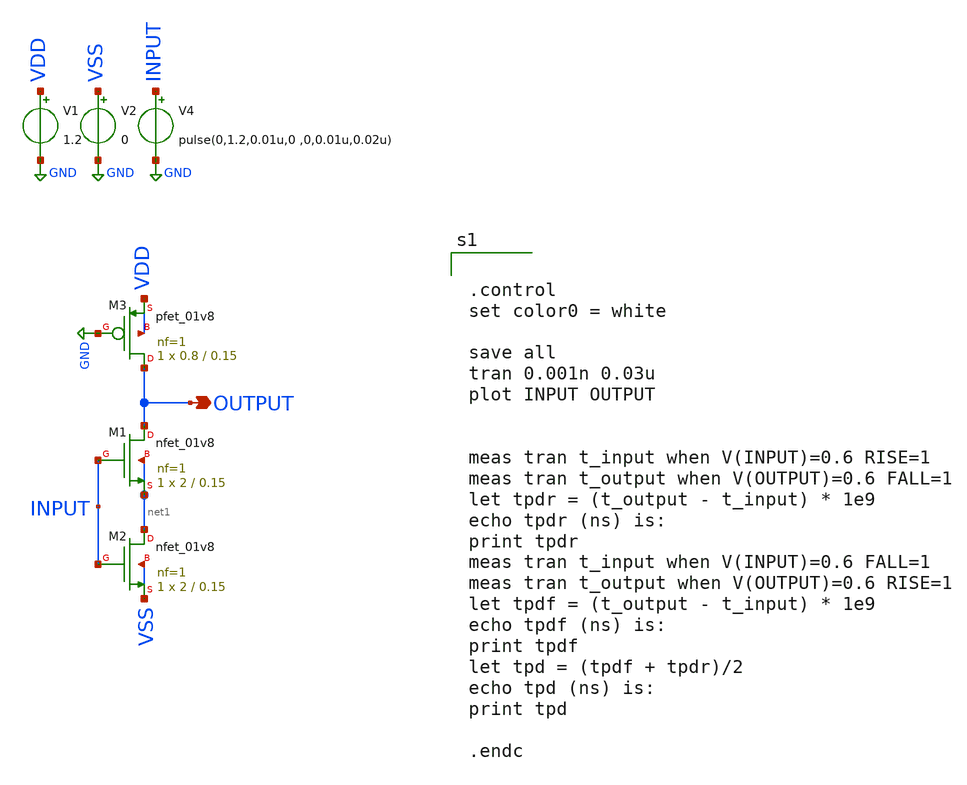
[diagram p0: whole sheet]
** sch_path: design/xschem/pseudo_nand2_tb.sch
**.subckt pseudo_nand2_tb OUTPUT
*.opin OUTPUT
V1 VDD GND 1.2
V2 VSS GND 0
V4 INPUT GND pulse(0,1.2,0.01u,0 ,0,0.01u,0.02u)
XM1 OUTPUT INPUT net1 net1 sky130_fd_pr__nfet_01v8 L=0.15 W=2 nf=1 ad='int((nf+1)/2) * W/nf * 0.29' as='int((nf+2)/2) * W/nf * 0.29'
+ pd='2*int((nf+1)/2) * (W/nf + 0.29)' ps='2*int((nf+2)/2) * (W/nf + 0.29)' nrd='0.29 / W' nrs='0.29 / W'
+ sa=0 sb=0 sd=0 mult=1 m=1
XM2 net1 INPUT VSS VSS sky130_fd_pr__nfet_01v8 L=0.15 W=2 nf=1 ad='int((nf+1)/2) * W/nf * 0.29' as='int((nf+2)/2) * W/nf * 0.29'
+ pd='2*int((nf+1)/2) * (W/nf + 0.29)' ps='2*int((nf+2)/2) * (W/nf + 0.29)' nrd='0.29 / W' nrs='0.29 / W'
+ sa=0 sb=0 sd=0 mult=1 m=1
XM3 OUTPUT GND VDD VDD sky130_fd_pr__pfet_01v8 L=0.15 W=0.8 nf=1 ad='int((nf+1)/2) * W/nf * 0.29' as='int((nf+2)/2) * W/nf * 0.29'
+ pd='2*int((nf+1)/2) * (W/nf + 0.29)' ps='2*int((nf+2)/2) * (W/nf + 0.29)' nrd='0.29 / W' nrs='0.29 / W'
+ sa=0 sb=0 sd=0 mult=1 m=1
**** begin user architecture code

** opencircuitdesign pdks install
.lib $::SKYWATER_MODELS/sky130.lib.spice tt_mm




.control
set color0 = white

save all
tran 0.001n 0.03u
plot INPUT OUTPUT


meas tran t_input when V(INPUT)=0.6 RISE=1
meas tran t_output when V(OUTPUT)=0.6 FALL=1
let tpdr = (t_output - t_input) * 1e9
echo tpdr (ns) is:
print tpdr
meas tran t_input when V(INPUT)=0.6 FALL=1
meas tran t_output when V(OUTPUT)=0.6 RISE=1
let tpdf = (t_output - t_input) * 1e9
echo tpdf (ns) is:
print tpdf
let tpd = (tpdf + tpdr)/2
echo tpd (ns) is:
print tpd

.endc


**** end user architecture code
**.ends
.GLOBAL GND
.end
